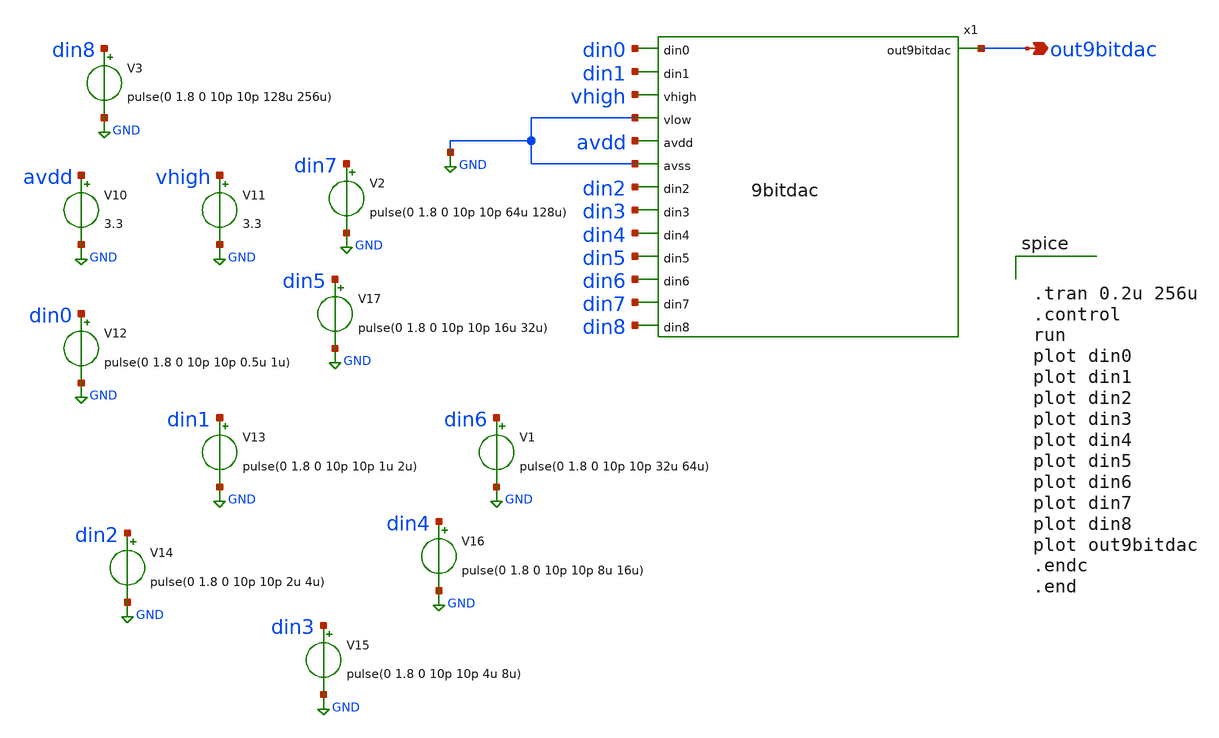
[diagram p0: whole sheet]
** sch_path: xschem/tb_9bitdac.sch
**.subckt tb_9bitdac out9bitdac
*.opin out9bitdac
x1 out9bitdac din0 din1 vhigh GND avdd GND din2 din3 din4 din5 din6 din7 din8 9bitdac
V10 avdd GND 3.3
V11 vhigh GND 3.3
V12 din0 GND pulse(0 1.8 0 10p 10p 0.5u 1u)
V13 din1 GND pulse(0 1.8 0 10p 10p 1u 2u)
V14 din2 GND pulse(0 1.8 0 10p 10p 2u 4u)
V15 din3 GND pulse(0 1.8 0 10p 10p 4u 8u)
V16 din4 GND pulse(0 1.8 0 10p 10p 8u 16u)
V17 din5 GND pulse(0 1.8 0 10p 10p 16u 32u)
V1 din6 GND pulse(0 1.8 0 10p 10p 32u 64u)
V2 din7 GND pulse(0 1.8 0 10p 10p 64u 128u)
V3 din8 GND pulse(0 1.8 0 10p 10p 128u 256u)
**** begin user architecture code

** opencircuitdesign pdks install
.lib $::SKYWATER_MODELS/sky130.lib.spice tt




.tran 0.2u 256u
.control
run
plot din0
plot din1
plot din2
plot din3
plot din4
plot din5
plot din6
plot din7
plot din8
plot out9bitdac
.endc
.end

**** end user architecture code
**.ends
.GLOBAL GND
.end
